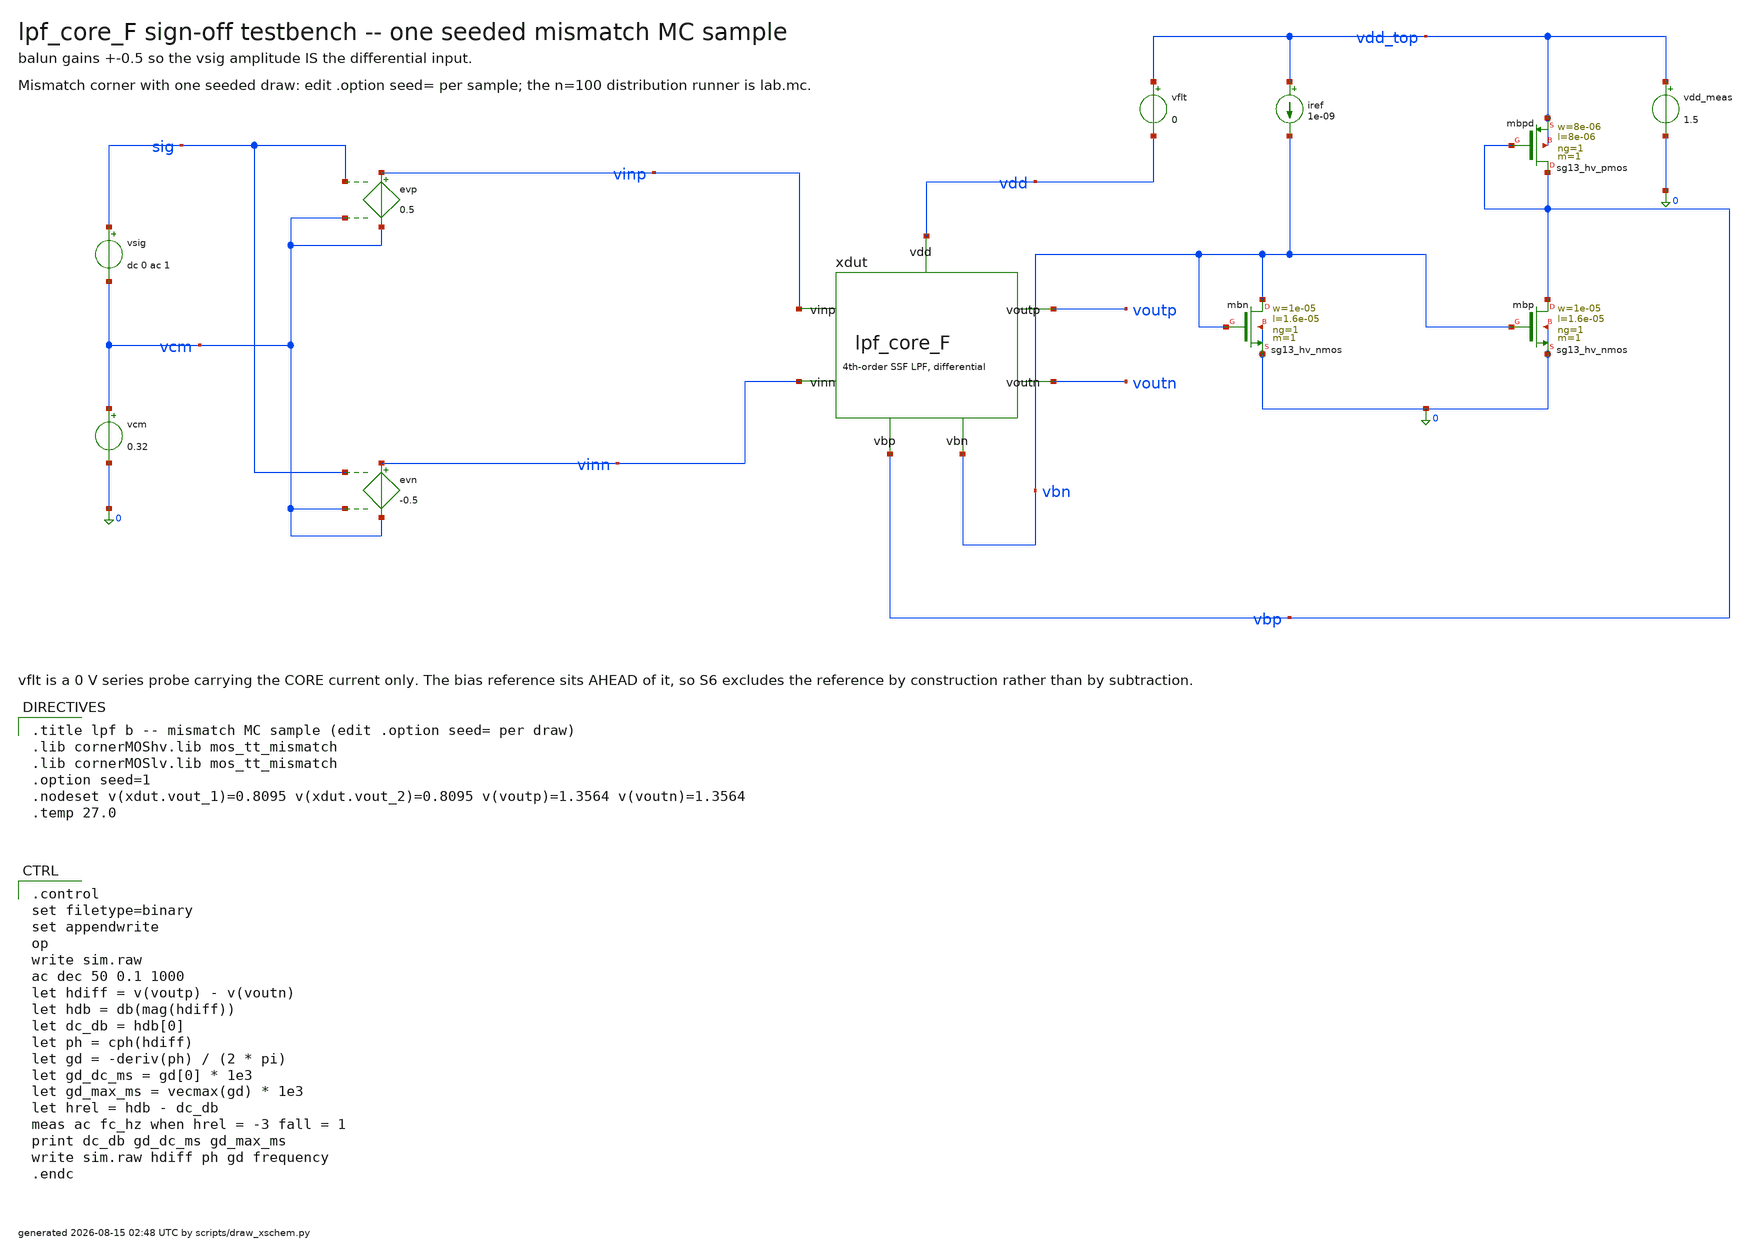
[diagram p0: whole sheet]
** sch_path: signoff/F-minnoise/lpf_tb_F_mc.sch
**.subckt lpf_tb_F_mc
vsig sig vcm dc 0 ac 1
vcm vcm 0 0.32
evp vinp vcm sig vcm 0.5
evn vinn vcm sig vcm -0.5
xdut vinp vinn voutp voutn vbn vbp vdd lpf_core_F
vflt vdd_top vdd 0
vdd_meas vdd_top 0 1.5
iref vdd_top vbn 1e-09
Xmbn vbn vbn 0 0 sg13_hv_nmos w=1e-05 l=1.6e-05 ng=1 m=1 mm_ok=1
Xmbp vbp vbn 0 0 sg13_hv_nmos w=1e-05 l=1.6e-05 ng=1 m=1 mm_ok=1
Xmbpd vbp vbp vdd_top vdd_top sg13_hv_pmos w=8e-06 l=8e-06 ng=1 m=1 mm_ok=1
**** begin user architecture code

.title lpf b -- mismatch MC sample (edit .option seed= per draw)
.lib cornerMOShv.lib mos_tt_mismatch
.lib cornerMOSlv.lib mos_tt_mismatch
.option seed=1
.nodeset v(xdut.vout_1)=0.8095 v(xdut.vout_2)=0.8095 v(voutp)=1.3564 v(voutn)=1.3564
.temp 27.0


.control
set filetype=binary
set appendwrite
op
write sim.raw
ac dec 50 0.1 1000
let hdiff = v(voutp) - v(voutn)
let hdb = db(mag(hdiff))
let dc_db = hdb[0]
let ph = cph(hdiff)
let gd = -deriv(ph) / (2 * pi)
let gd_dc_ms = gd[0] * 1e3
let gd_max_ms = vecmax(gd) * 1e3
let hrel = hdb - dc_db
meas ac fc_hz when hrel = -3 fall = 1
print dc_db gd_dc_ms gd_max_ms
write sim.raw hdiff ph gd frequency
.endc

**** end user architecture code
**.ends
.end
